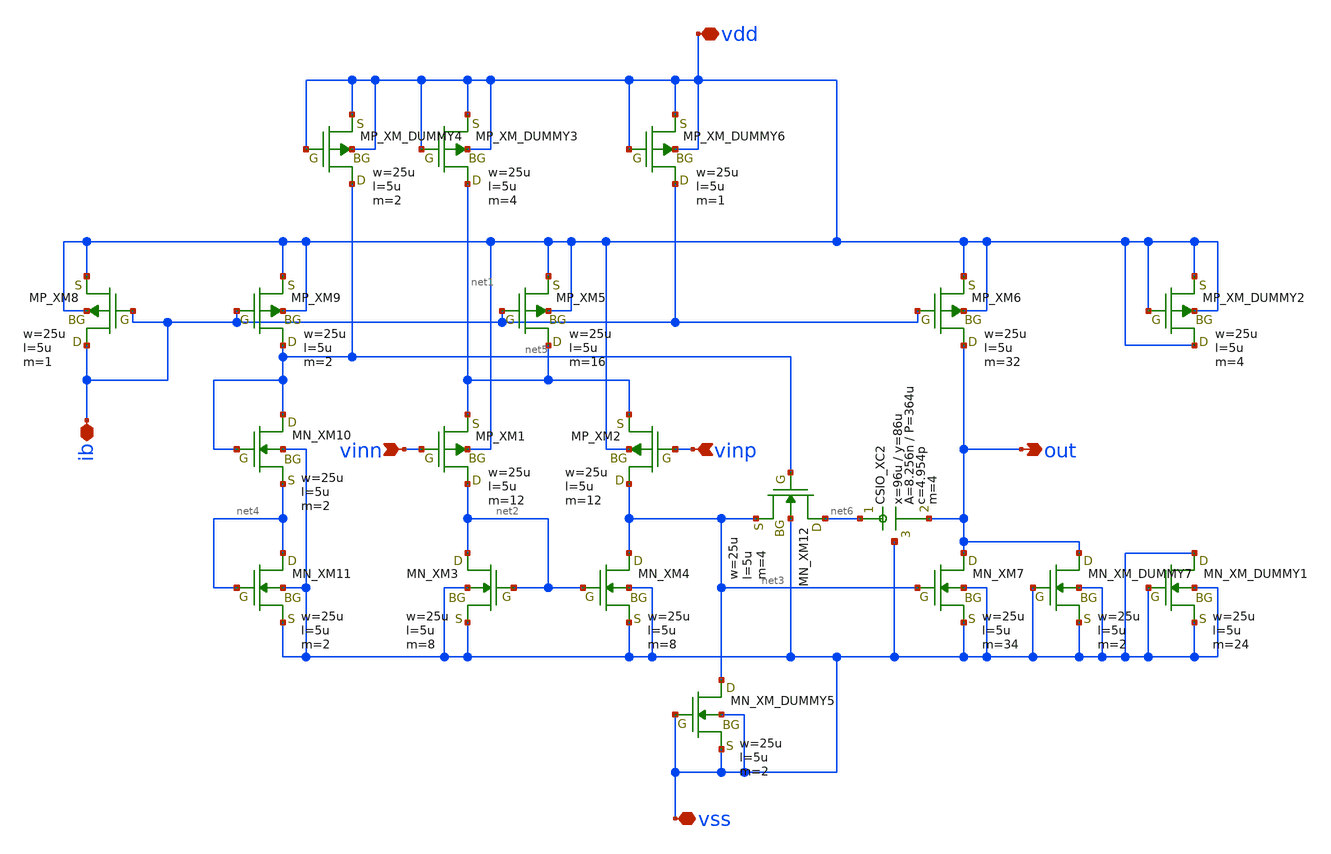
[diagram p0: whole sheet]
** sch_path: member_project/opamp/cat_nekonekone/opamp_test.sch
**.subckt opamp_test vinn vinp out ib vss vdd
*.ipin vinn
*.ipin vinp
*.opin out
*.iopin ib
*.iopin vss
*.iopin vdd
XXM1 net2 vinn net1 vdd PMOS w=25u l=5u nrd=0 nrs=0 m=12
XXM4 net3 net2 vss vss NMOS w=25u l=5u nrd=0 nrs=0 m=8
XXM2 net3 vinp net1 vdd PMOS w=25u l=5u nrd=0 nrs=0 m=12
XXM3 net2 net2 vss vss NMOS w=25u l=5u nrd=0 nrs=0 m=8
XXM5 net1 ib vdd vdd PMOS w=25u l=5u nrd=0 nrs=0 m=16
XXM6 out ib vdd vdd PMOS w=25u l=5u nrd=0 nrs=0 m=32
XXM7 out net3 vss vss NMOS w=25u l=5u nrd=0 nrs=0 m=34
XXM8 ib ib vdd vdd PMOS w=25u l=5u nrd=0 nrs=0 m=1
XXM9 net5 ib vdd vdd PMOS w=25u l=5u nrd=0 nrs=0 m=2
XXM10 net5 net5 net4 vss NMOS w=25u l=5u nrd=0 nrs=0 m=2
XXM11 net4 net4 vss vss NMOS w=25u l=5u nrd=0 nrs=0 m=2
XXM12 net6 net5 net3 vss NMOS w=25u l=5u nrd=0 nrs=0 m=4
XXM_DUMMY2 vdd vdd vdd vdd PMOS w=25u l=5u nrd=0 nrs=0 m=4
XXM_DUMMY1 vss vss vss vss NMOS w=25u l=5u nrd=0 nrs=0 m=24
XXM_DUMMY3 net1 vdd vdd vdd PMOS w=25u l=5u nrd=0 nrs=0 m=4
XXM_DUMMY5 net3 vss vss vss NMOS w=25u l=5u nrd=0 nrs=0 m=2
XXM_DUMMY4 net5 vdd vdd vdd PMOS w=25u l=5u nrd=0 nrs=0 m=2
XXM_DUMMY6 ib vdd vdd vdd PMOS w=25u l=5u nrd=0 nrs=0 m=1
XXM_DUMMY7 out vss vss vss NMOS w=25u l=5u nrd=0 nrs=0 m=2
XXC2 net6 out vss F_CSIO c=4.954p x=96u y=86u m=4
**.ends
.end
